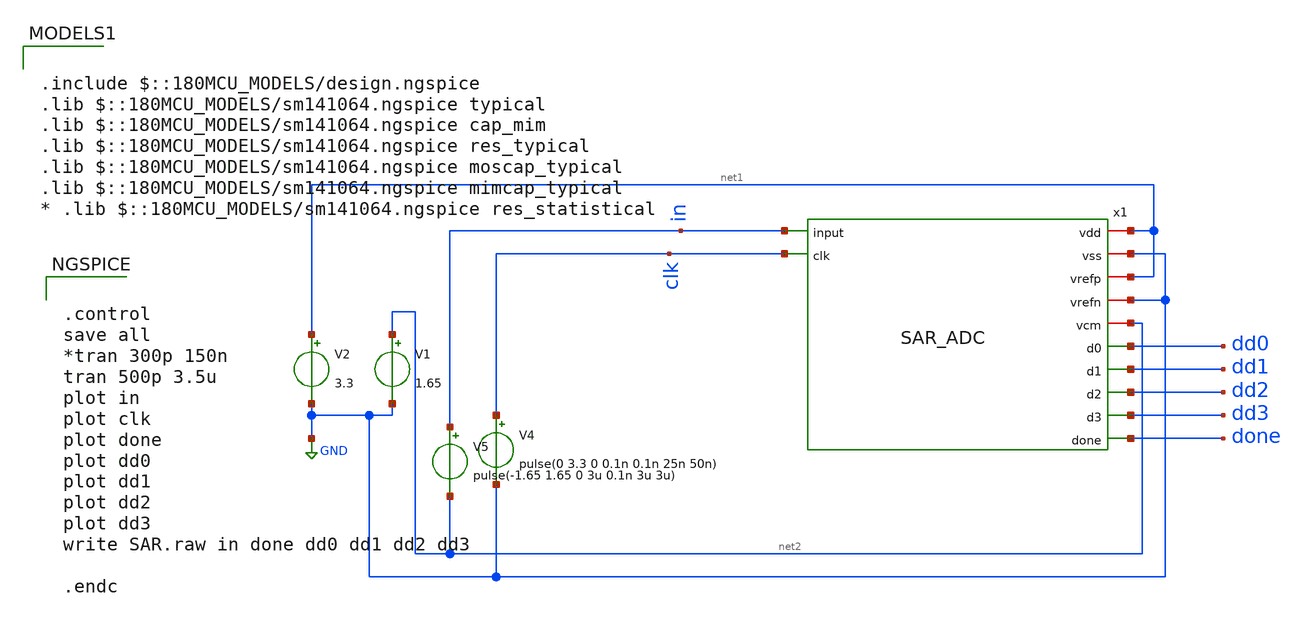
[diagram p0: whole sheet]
** sch_path: member_project/ice458/dynamic_comparator/xschem/SAR_ADC_tb.sch
**.subckt SAR_ADC_tb
x1 net1 GND net1 GND net2 in clk dd0 dd1 dd2 dd3 done SAR_ADC
V2 net1 GND 3.3
V1 net2 GND 1.65
V5 in net2 pulse(-1.65 1.65 0 3u 0.1n 3u 3u)
V4 clk GND pulse(0 3.3 0 0.1n 0.1n 25n 50n)
**** begin user architecture code


.control
save all
*tran 300p 150n
tran 500p 3.5u
plot in
plot clk
plot done
plot dd0
plot dd1
plot dd2
plot dd3
write SAR.raw in done dd0 dd1 dd2 dd3

.endc



.include $::180MCU_MODELS/design.ngspice
.lib $::180MCU_MODELS/sm141064.ngspice typical
.lib $::180MCU_MODELS/sm141064.ngspice cap_mim
.lib $::180MCU_MODELS/sm141064.ngspice res_typical
.lib $::180MCU_MODELS/sm141064.ngspice moscap_typical
.lib $::180MCU_MODELS/sm141064.ngspice mimcap_typical
* .lib $::180MCU_MODELS/sm141064.ngspice res_statistical

**** end user architecture code
**.ends
.GLOBAL GND
.end
